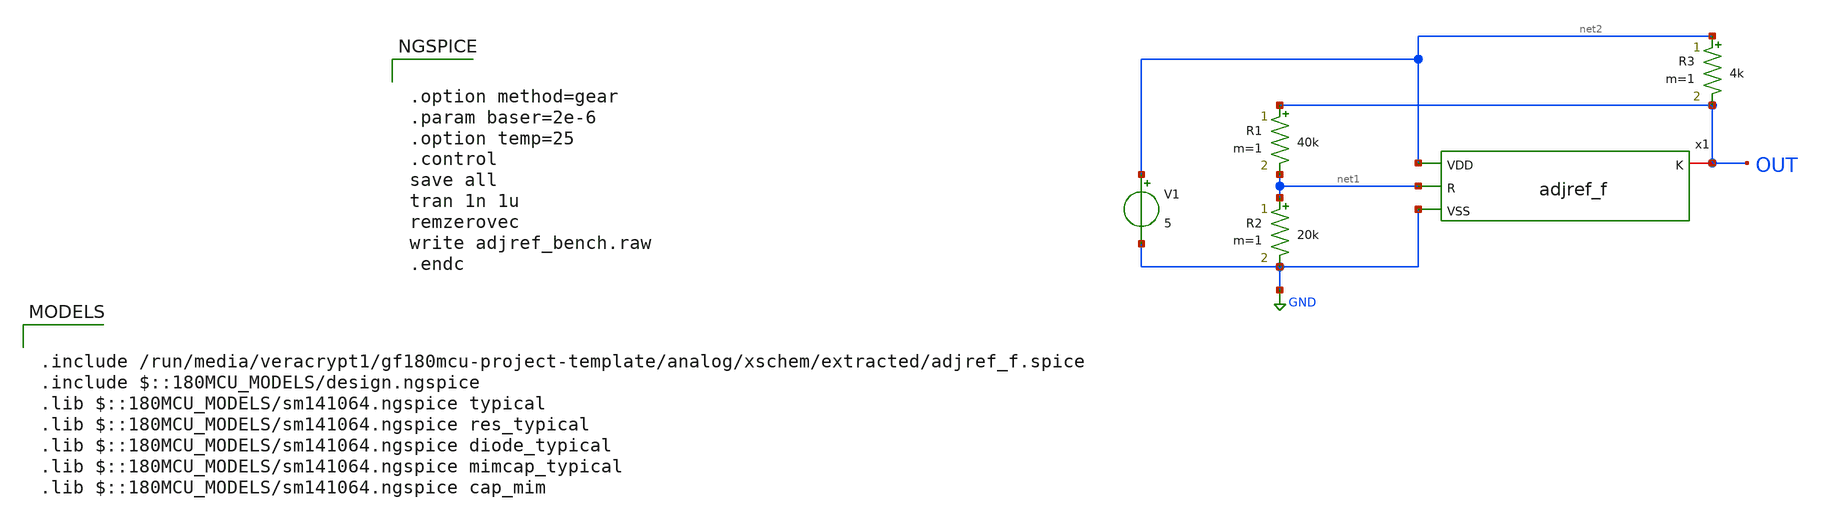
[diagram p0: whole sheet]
** sch_path: analog/xschem/adjref_bench.sch
**.subckt adjref_bench
R1 OUT net1 40k m=1
R2 net1 GND 20k m=1
V1 net2 GND 5
R3 net2 OUT 4k m=1
x1 net2 GND net1 OUT adjref_f
**** begin user architecture code


.option method=gear
.param baser=2e-6
.option temp=25
.control
save all
tran 1n 1u
remzerovec
write adjref_bench.raw
.endc



.include /run/media/veracrypt1/gf180mcu-project-template/analog/xschem/extracted/adjref_f.spice
.include $::180MCU_MODELS/design.ngspice
.lib $::180MCU_MODELS/sm141064.ngspice typical
.lib $::180MCU_MODELS/sm141064.ngspice res_typical
.lib $::180MCU_MODELS/sm141064.ngspice diode_typical
.lib $::180MCU_MODELS/sm141064.ngspice mimcap_typical
.lib $::180MCU_MODELS/sm141064.ngspice cap_mim

**** end user architecture code
**.ends
.GLOBAL GND
.end
